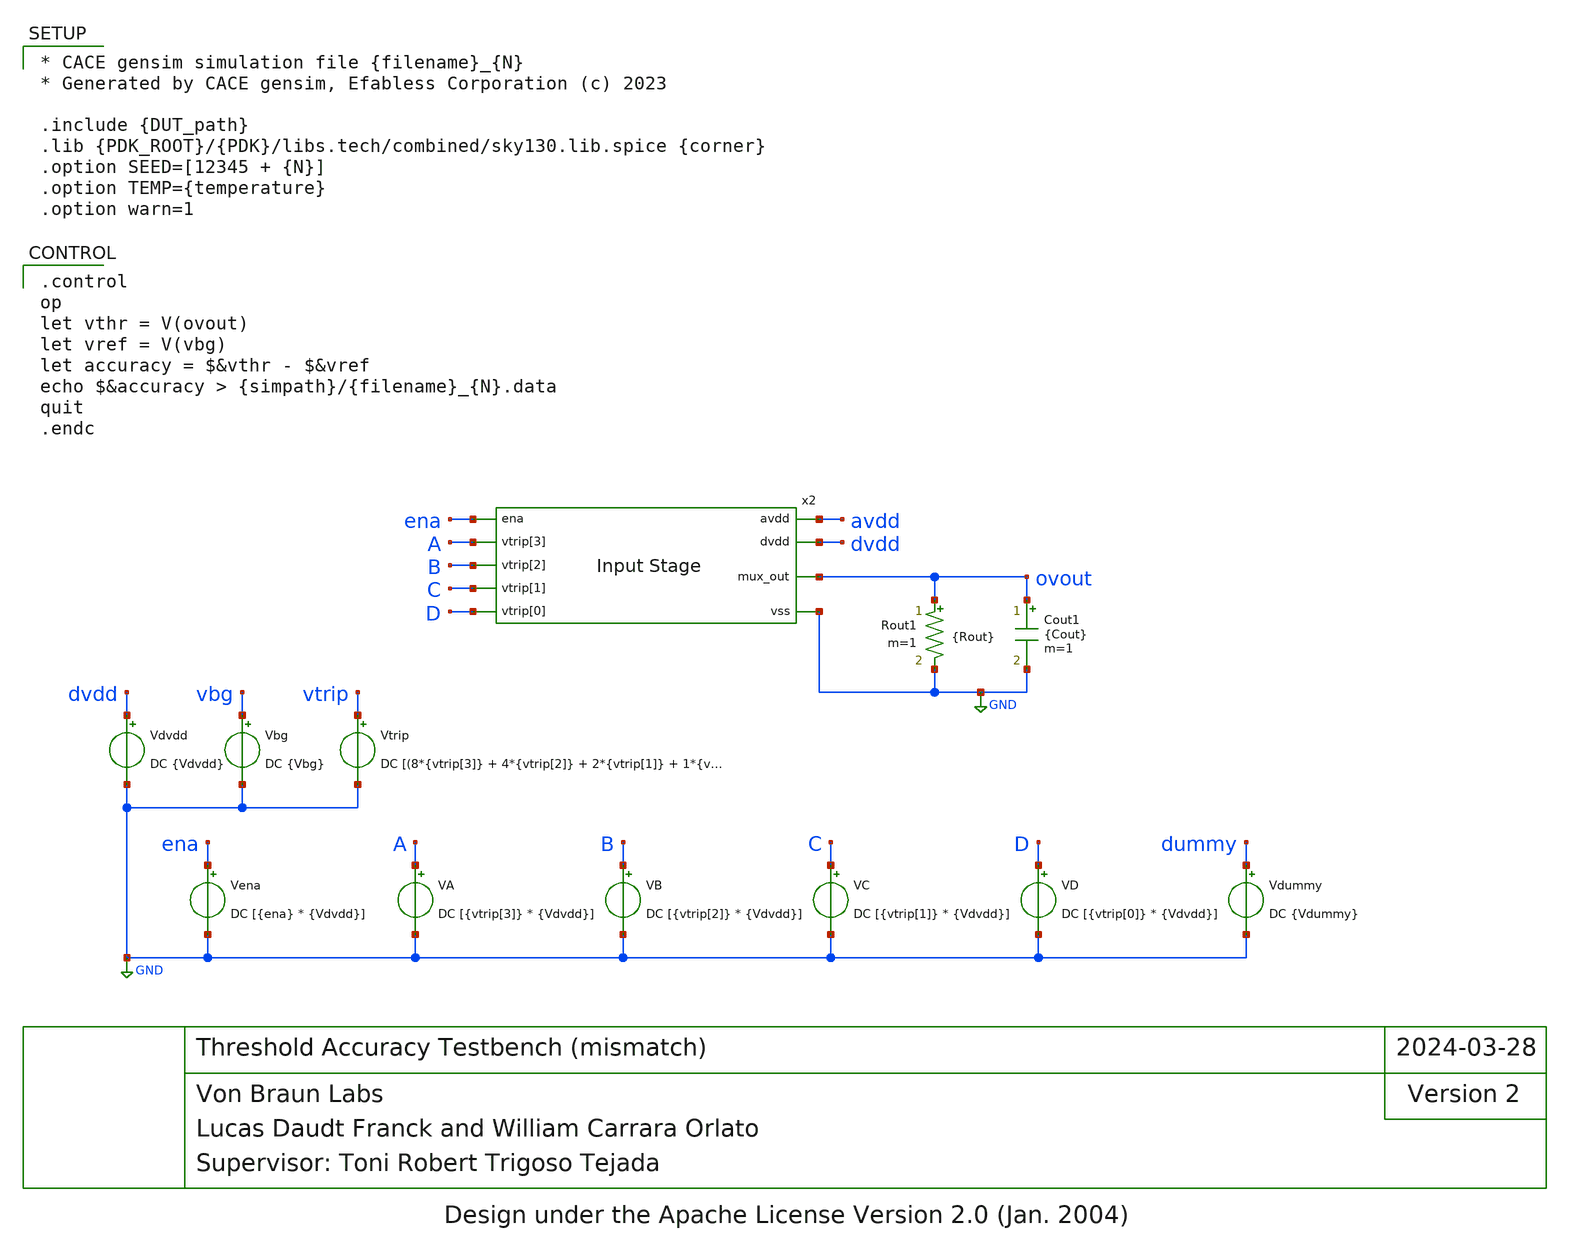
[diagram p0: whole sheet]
** sch_path: blocks/input/cace/tb_vacc_mm.sch
* Design under the Apache License Version 2.0 (Jan. 2004)
**.subckt tb_vacc_mm
Vena ena GND DC [{ena} * {Vdvdd}]
VA A GND DC [{vtrip[3]} * {Vdvdd}]
VB B GND DC [{vtrip[2]} * {Vdvdd}]
VC C GND DC [{vtrip[1]} * {Vdvdd}]
VD D GND DC [{vtrip[0]} * {Vdvdd}]
Vdummy dummy GND DC {Vdummy}
Vdvdd dvdd GND DC {Vdvdd}
Vbg vbg GND DC {Vbg}
Vtrip vtrip GND DC [(8*{vtrip[3]} + 4*{vtrip[2]} + 2*{vtrip[1]} + 1*{vtrip[0]})*0.14667 + 3.3]
Cout1 ovout GND {Cout} m=1
Rout1 ovout GND {Rout} m=1
x2 avdd dvdd ena A GND B ovout C D input
**** begin user architecture code

* CACE gensim simulation file {filename}_{N}
* Generated by CACE gensim, Efabless Corporation (c) 2023

.include {DUT_path}
.lib {PDK_ROOT}/{PDK}/libs.tech/combined/sky130.lib.spice {corner}
.option SEED=[12345 + {N}]
.option TEMP={temperature}
.option warn=1



.control
op
let vthr = V(ovout)
let vref = V(vbg)
let accuracy = $&vthr - $&vref
echo $&accuracy > {simpath}/{filename}_{N}.data
quit
.endc


**** end user architecture code
**.ends
.GLOBAL GND
.end
